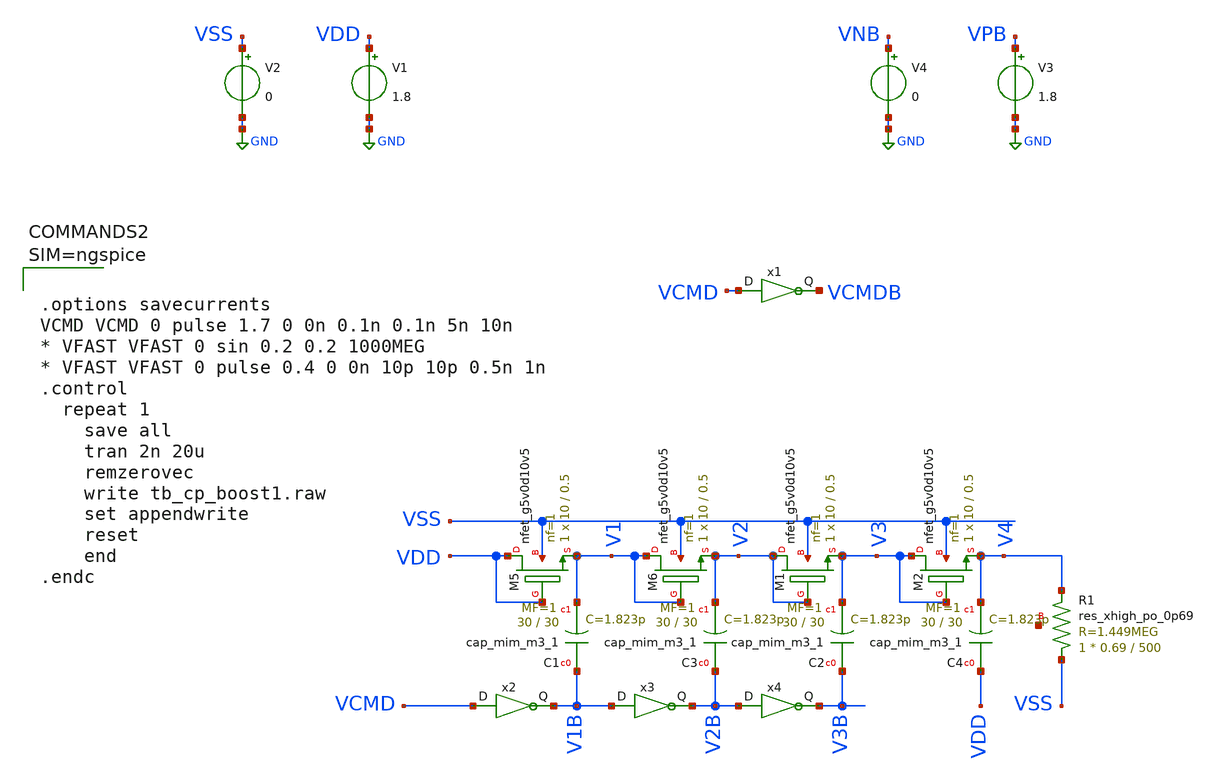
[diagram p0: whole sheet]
** sch_path: xschem/tb_cp_boost1.sch
**.subckt tb_cp_boost1
V1 VDD GND 1.8
V2 VSS GND 0
V3 VPB GND 1.8
V4 VNB GND 0
x1 VCMD VCMDB VDD VSS pll_inv1
XM5 VDD VDD V1 VSS sky130_fd_pr__nfet_g5v0d10v5 L=0.5 W=10 nf=1 ad='int((nf+1)/2) * W/nf * 0.29' as='int((nf+2)/2) * W/nf * 0.29'
+ pd='2*int((nf+1)/2) * (W/nf + 0.29)' ps='2*int((nf+2)/2) * (W/nf + 0.29)' nrd='0.29 / W' nrs='0.29 / W'
+ sa=0 sb=0 sd=0 mult=1 m=1
XC1 V1B V1 sky130_fd_pr__cap_mim_m3_1 W=30 L=30 MF=1 m=1
XM6 V1 V1 V2 VSS sky130_fd_pr__nfet_g5v0d10v5 L=0.5 W=10 nf=1 ad='int((nf+1)/2) * W/nf * 0.29' as='int((nf+2)/2) * W/nf * 0.29'
+ pd='2*int((nf+1)/2) * (W/nf + 0.29)' ps='2*int((nf+2)/2) * (W/nf + 0.29)' nrd='0.29 / W' nrs='0.29 / W'
+ sa=0 sb=0 sd=0 mult=1 m=1
XC3 V2B V2 sky130_fd_pr__cap_mim_m3_1 W=30 L=30 MF=1 m=1
XM1 V2 V2 V3 VSS sky130_fd_pr__nfet_g5v0d10v5 L=0.5 W=10 nf=1 ad='int((nf+1)/2) * W/nf * 0.29' as='int((nf+2)/2) * W/nf * 0.29'
+ pd='2*int((nf+1)/2) * (W/nf + 0.29)' ps='2*int((nf+2)/2) * (W/nf + 0.29)' nrd='0.29 / W' nrs='0.29 / W'
+ sa=0 sb=0 sd=0 mult=1 m=1
XC2 V3B V3 sky130_fd_pr__cap_mim_m3_1 W=30 L=30 MF=1 m=1
XM2 V3 V3 V4 VSS sky130_fd_pr__nfet_g5v0d10v5 L=0.5 W=10 nf=1 ad='int((nf+1)/2) * W/nf * 0.29' as='int((nf+2)/2) * W/nf * 0.29'
+ pd='2*int((nf+1)/2) * (W/nf + 0.29)' ps='2*int((nf+2)/2) * (W/nf + 0.29)' nrd='0.29 / W' nrs='0.29 / W'
+ sa=0 sb=0 sd=0 mult=1 m=1
XC4 VDD V4 sky130_fd_pr__cap_mim_m3_1 W=30 L=30 MF=1 m=1
x2 VCMD V1B VDD VSS pll_inv1
x3 V1B V2B VDD VSS pll_inv1
x4 V2B V3B VDD VSS pll_inv1
XR1 VSS V4 net1 sky130_fd_pr__res_xhigh_po_0p69 L=500 mult=1 m=1
**** begin user architecture code

** opencircuitdesign pdks install
.lib $::SKYWATER_MODELS/sky130.lib.spice tt_mm





.options savecurrents
VCMD VCMD 0 pulse 1.7 0 0n 0.1n 0.1n 5n 10n
* VFAST VFAST 0 sin 0.2 0.2 1000MEG
* VFAST VFAST 0 pulse 0.4 0 0n 10p 10p 0.5n 1n
.control
  repeat 1
    save all
    tran 2n 20u
    remzerovec
    write tb_cp_boost1.raw
    set appendwrite
    reset
    end
.endc



**** end user architecture code
**.ends

* expanding   symbol:  pll_inv1.sym # of pins=2
** sym_path: xschem/pll_inv1.sym
** sch_path: xschem/pll_inv1.sch
.subckt pll_inv1 D Q VDD VSS
*.opin Q
*.ipin D
*.ipin VDD
*.ipin VSS
XM3 Q D net1 net1 sky130_fd_pr__pfet_01v8_lvt L=0.5 W=1 nf=1 ad='int((nf+1)/2) * W/nf * 0.29' as='int((nf+2)/2) * W/nf * 0.29'
+ pd='2*int((nf+1)/2) * (W/nf + 0.29)' ps='2*int((nf+2)/2) * (W/nf + 0.29)' nrd='0.29 / W' nrs='0.29 / W'
+ sa=0 sb=0 sd=0 mult=1 m=1
vpwr VDD net1 0
.save i(vpwr)
XM1 Q D VSS VSS sky130_fd_pr__nfet_01v8_lvt L=0.25 W=0.5 nf=1 ad='int((nf+1)/2) * W/nf * 0.29' as='int((nf+2)/2) * W/nf * 0.29'
+ pd='2*int((nf+1)/2) * (W/nf + 0.29)' ps='2*int((nf+2)/2) * (W/nf + 0.29)' nrd='0.29 / W' nrs='0.29 / W'
+ sa=0 sb=0 sd=0 mult=1 m=1
.ends

.GLOBAL GND
.end
